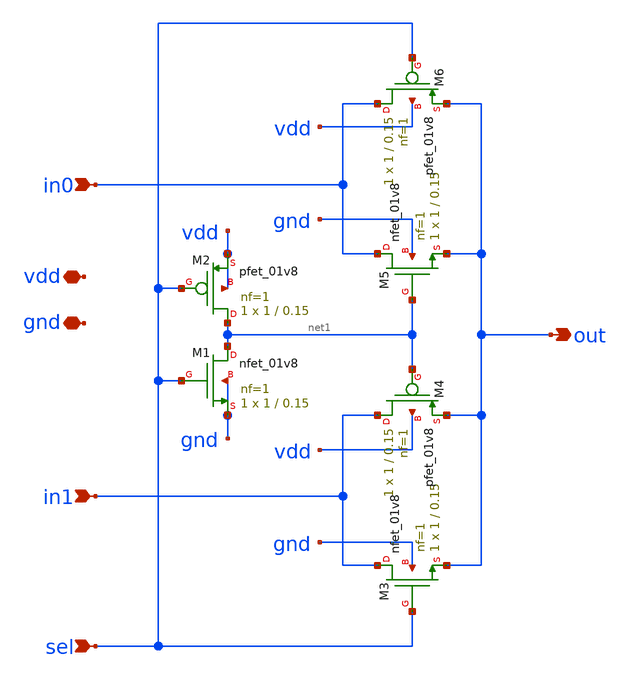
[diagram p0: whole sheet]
** sch_path: Primitives/Multiplexer 2to1/Xschem Files/sky130_mux.sch
**.subckt sky130_mux vdd gnd in0 sel in1 out
*.iopin vdd
*.iopin gnd
*.ipin in0
*.ipin sel
*.ipin in1
*.opin out
XM1 net1 sel gnd gnd sky130_fd_pr__nfet_01v8 L=0.15 W=1 nf=1 ad='int((1 + 1)/2) * 1 / 1 * 0.29' as='int((1 + 2)/2) * 1 / 1 * 0.29'
+ pd='2*int((1 + 1)/2) * (1 / 1 + 0.29)' ps='2*int((1 + 2)/2) * (1 / 1 + 0.29)' nrd='0.29 / 1 ' nrs='0.29 / 1 '
+ sa=0 sb=0 sd=0 mult=1 m=1
XM2 net1 sel vdd vdd sky130_fd_pr__pfet_01v8 L=0.15 W=1 nf=1 ad='int((1 + 1)/2) * 1 / 1 * 0.29' as='int((1 + 2)/2) * 1 / 1 * 0.29'
+ pd='2*int((1 + 1)/2) * (1 / 1 + 0.29)' ps='2*int((1 + 2)/2) * (1 / 1 + 0.29)' nrd='0.29 / 1 ' nrs='0.29 / 1 '
+ sa=0 sb=0 sd=0 mult=1 m=1
XM3 in1 sel out gnd sky130_fd_pr__nfet_01v8 L=0.15 W=1 nf=1 ad='int((1 + 1)/2) * 1 / 1 * 0.29' as='int((1 + 2)/2) * 1 / 1 * 0.29'
+ pd='2*int((1 + 1)/2) * (1 / 1 + 0.29)' ps='2*int((1 + 2)/2) * (1 / 1 + 0.29)' nrd='0.29 / 1 ' nrs='0.29 / 1 '
+ sa=0 sb=0 sd=0 mult=1 m=1
XM4 in1 net1 out vdd sky130_fd_pr__pfet_01v8 L=0.15 W=1 nf=1 ad='int((1 + 1)/2) * 1 / 1 * 0.29' as='int((1 + 2)/2) * 1 / 1 * 0.29'
+ pd='2*int((1 + 1)/2) * (1 / 1 + 0.29)' ps='2*int((1 + 2)/2) * (1 / 1 + 0.29)' nrd='0.29 / 1 ' nrs='0.29 / 1 '
+ sa=0 sb=0 sd=0 mult=1 m=1
XM5 in0 net1 out gnd sky130_fd_pr__nfet_01v8 L=0.15 W=1 nf=1 ad='int((1 + 1)/2) * 1 / 1 * 0.29' as='int((1 + 2)/2) * 1 / 1 * 0.29'
+ pd='2*int((1 + 1)/2) * (1 / 1 + 0.29)' ps='2*int((1 + 2)/2) * (1 / 1 + 0.29)' nrd='0.29 / 1 ' nrs='0.29 / 1 '
+ sa=0 sb=0 sd=0 mult=1 m=1
XM6 in0 sel out vdd sky130_fd_pr__pfet_01v8 L=0.15 W=1 nf=1 ad='int((1 + 1)/2) * 1 / 1 * 0.29' as='int((1 + 2)/2) * 1 / 1 * 0.29'
+ pd='2*int((1 + 1)/2) * (1 / 1 + 0.29)' ps='2*int((1 + 2)/2) * (1 / 1 + 0.29)' nrd='0.29 / 1 ' nrs='0.29 / 1 '
+ sa=0 sb=0 sd=0 mult=1 m=1
**.ends
.end
